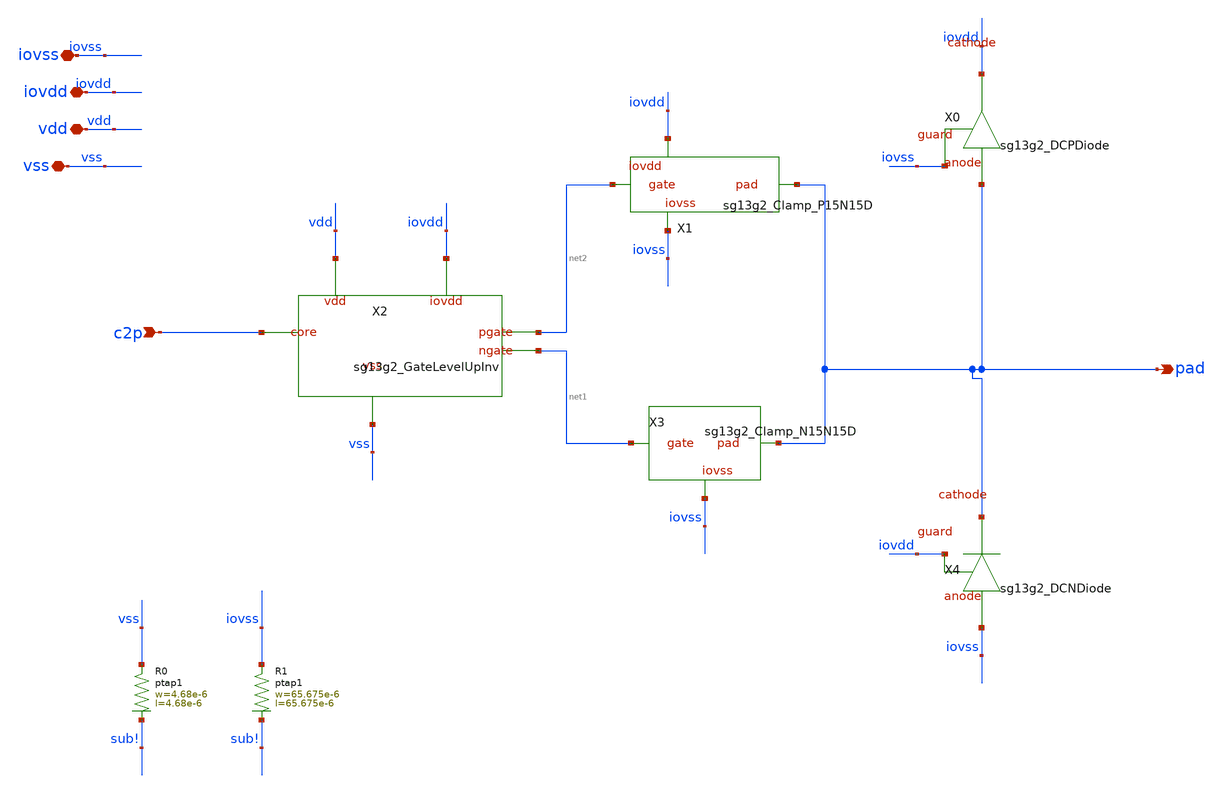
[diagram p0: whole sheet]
** sch_path: ihp-sg13g2/libs.ref/sg13g2_io/sch/xschem/sg13g2_IOPadOut30mA.sch
**.subckt sg13g2_IOPadOut30mA vdd vss iovdd c2p pad iovss
*.iopin vdd
*.iopin vss
*.iopin iovdd
*.ipin c2p
*.opin pad
*.iopin iovss
X0 iovss iovdd pad sg13g2_DCPDiode
X1 pad net2 iovss iovdd sg13g2_Clamp_P15N15D
X2 c2p net2 net1 vss vdd iovdd sg13g2_GateLevelUpInv
X3 pad net1 iovss sg13g2_Clamp_N15N15D
X4 iovdd pad iovss sg13g2_DCNDiode
XR0 vss sub! ptap1 R=24.12 w=4.68e-6 l=4.68e-6
XR1 iovss sub! ptap1 R=214.2m w=65.675e-6 l=65.675e-6
**.ends
.end
